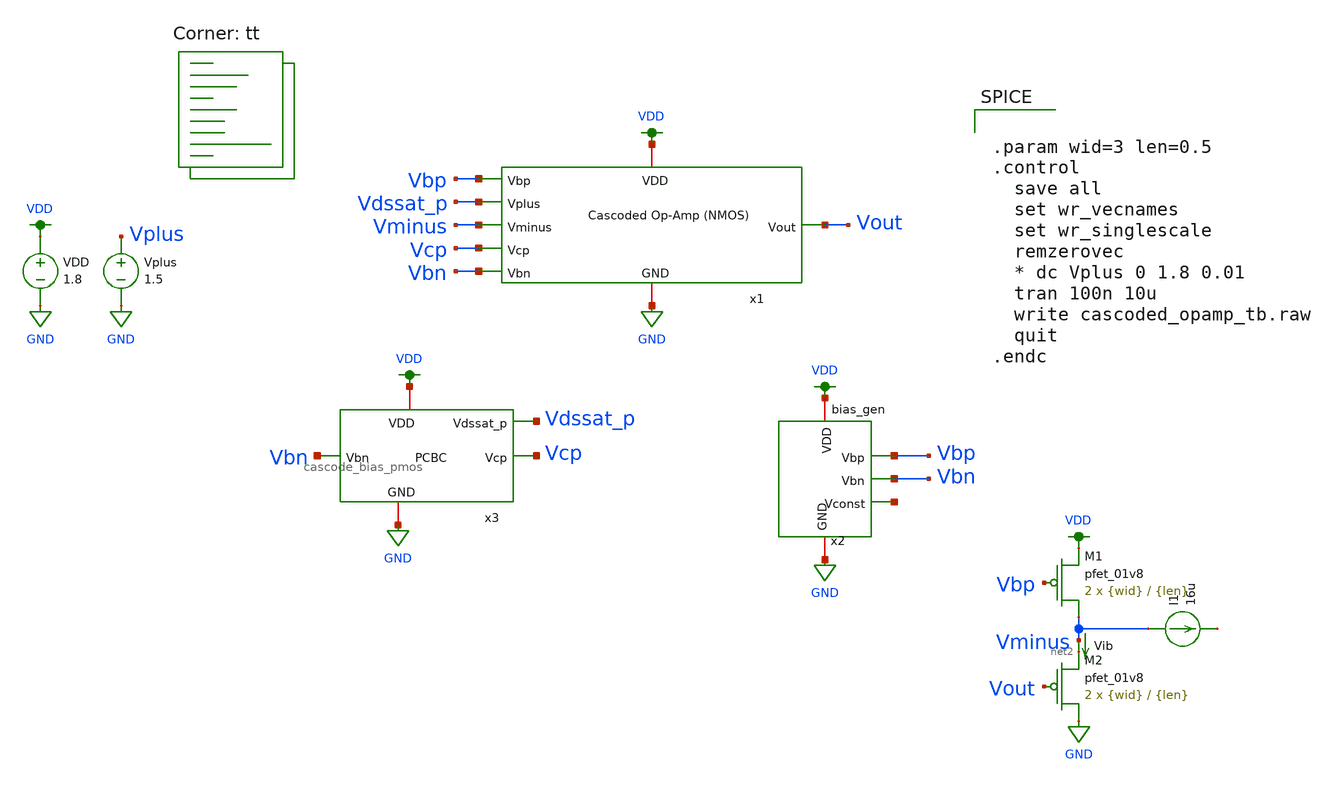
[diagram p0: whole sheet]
** sch_path: final/schematics/cascoded_opamp_tb.sch
**.subckt cascoded_opamp_tb
x1 Vbp Vdssat_p Vminus Vcp Vbn VDD GND Vout cascoded_opamp
VDD VDD GND 1.8
x3 Vbn VDD GND Vcp Vdssat_p cascode_bias_pmos
x2 VDD Vbp net1 GND Vbn bias_gen
XM1 Vminus Vbp VDD VDD sky130_fd_pr__pfet_01v8 L={len} W={wid} nf=1 ad='int((nf+1)/2) * W/nf * 0.29'
+ as='int((nf+2)/2) * W/nf * 0.29' pd='2*int((nf+1)/2) * (W/nf + 0.29)' ps='2*int((nf+2)/2) * (W/nf + 0.29)'
+ nrd='0.29 / W' nrs='0.29 / W' sa=0 sb=0 sd=0 mult=2 m=2
XM2 GND Vout net2 VDD sky130_fd_pr__pfet_01v8 L={len} W={wid} nf=1 ad='int((nf+1)/2) * W/nf * 0.29' as='int((nf+2)/2) * W/nf * 0.29'
+ pd='2*int((nf+1)/2) * (W/nf + 0.29)' ps='2*int((nf+2)/2) * (W/nf + 0.29)' nrd='0.29 / W' nrs='0.29 / W'
+ sa=0 sb=0 sd=0 mult=2 m=2
Vib Vminus net2 0
.save i(vib)
Vplus Vplus GND 1.5
I1 Vminus net3 16u
**** begin user architecture code
.lib $::SKYWATER_MODELS/sky130.lib.spice tt


.param wid=3 len=0.5
.control
  save all
  set wr_vecnames
  set wr_singlescale
  remzerovec
  * dc Vplus 0 1.8 0.01
  tran 100n 10u
  write cascoded_opamp_tb.raw
  quit
.endc


**** end user architecture code
**.ends

* expanding   symbol:  cascoded_opamp.sym # of pins=8
** sym_path: final/schematics/cascoded_opamp.sym
** sch_path: final/schematics/cascoded_opamp.sch
.subckt cascoded_opamp Vbp Vplus Vminus Vcp Vbn VDD GND Vout
*.ipin Vbp
*.ipin Vplus
*.ipin Vminus
*.ipin Vcp
*.ipin Vbn
*.iopin VDD
*.iopin GND
*.opin Vout
XM1 net1 Vbn GND GND sky130_fd_pr__nfet_01v8 L=0.15 W=1 nf=1 ad='int((nf+1)/2) * W/nf * 0.29' as='int((nf+2)/2) * W/nf * 0.29'
+ pd='2*int((nf+1)/2) * (W/nf + 0.29)' ps='2*int((nf+2)/2) * (W/nf + 0.29)' nrd='0.29 / W' nrs='0.29 / W'
+ sa=0 sb=0 sd=0 mult=1 m=1
XM2 net2 Vminus net1 GND sky130_fd_pr__nfet_01v8 L=0.15 W=1 nf=1 ad='int((nf+1)/2) * W/nf * 0.29' as='int((nf+2)/2) * W/nf * 0.29'
+ pd='2*int((nf+1)/2) * (W/nf + 0.29)' ps='2*int((nf+2)/2) * (W/nf + 0.29)' nrd='0.29 / W' nrs='0.29 / W'
+ sa=0 sb=0 sd=0 mult=1 m=1
XM3 net1 Vplus net3 GND sky130_fd_pr__nfet_01v8 L=0.15 W=1 nf=1 ad='int((nf+1)/2) * W/nf * 0.29' as='int((nf+2)/2) * W/nf * 0.29'
+ pd='2*int((nf+1)/2) * (W/nf + 0.29)' ps='2*int((nf+2)/2) * (W/nf + 0.29)' nrd='0.29 / W' nrs='0.29 / W'
+ sa=0 sb=0 sd=0 mult=1 m=1
XM4 net2 Vbp VDD VDD sky130_fd_pr__pfet_01v8 L=0.15 W=1 nf=1 ad='int((nf+1)/2) * W/nf * 0.29' as='int((nf+2)/2) * W/nf * 0.29'
+ pd='2*int((nf+1)/2) * (W/nf + 0.29)' ps='2*int((nf+2)/2) * (W/nf + 0.29)' nrd='0.29 / W' nrs='0.29 / W'
+ sa=0 sb=0 sd=0 mult=1 m=1
XM5 net3 Vbp VDD VDD sky130_fd_pr__pfet_01v8 L=0.15 W=1 nf=1 ad='int((nf+1)/2) * W/nf * 0.29' as='int((nf+2)/2) * W/nf * 0.29'
+ pd='2*int((nf+1)/2) * (W/nf + 0.29)' ps='2*int((nf+2)/2) * (W/nf + 0.29)' nrd='0.29 / W' nrs='0.29 / W'
+ sa=0 sb=0 sd=0 mult=1 m=1
XM6 net4 Vcp net2 VDD sky130_fd_pr__pfet_01v8 L=0.15 W=1 nf=1 ad='int((nf+1)/2) * W/nf * 0.29' as='int((nf+2)/2) * W/nf * 0.29'
+ pd='2*int((nf+1)/2) * (W/nf + 0.29)' ps='2*int((nf+2)/2) * (W/nf + 0.29)' nrd='0.29 / W' nrs='0.29 / W'
+ sa=0 sb=0 sd=0 mult=1 m=1
XM7 Vout Vcp net3 VDD sky130_fd_pr__pfet_01v8 L=0.15 W=1 nf=1 ad='int((nf+1)/2) * W/nf * 0.29' as='int((nf+2)/2) * W/nf * 0.29'
+ pd='2*int((nf+1)/2) * (W/nf + 0.29)' ps='2*int((nf+2)/2) * (W/nf + 0.29)' nrd='0.29 / W' nrs='0.29 / W'
+ sa=0 sb=0 sd=0 mult=1 m=1
XM8 GND net4 net4 GND sky130_fd_pr__nfet_01v8 L=0.15 W=1 nf=1 ad='int((nf+1)/2) * W/nf * 0.29' as='int((nf+2)/2) * W/nf * 0.29'
+ pd='2*int((nf+1)/2) * (W/nf + 0.29)' ps='2*int((nf+2)/2) * (W/nf + 0.29)' nrd='0.29 / W' nrs='0.29 / W'
+ sa=0 sb=0 sd=0 mult=1 m=1
XM9 Vout net4 GND GND sky130_fd_pr__nfet_01v8 L=0.15 W=1 nf=1 ad='int((nf+1)/2) * W/nf * 0.29' as='int((nf+2)/2) * W/nf * 0.29'
+ pd='2*int((nf+1)/2) * (W/nf + 0.29)' ps='2*int((nf+2)/2) * (W/nf + 0.29)' nrd='0.29 / W' nrs='0.29 / W'
+ sa=0 sb=0 sd=0 mult=1 m=1
.ends


* expanding   symbol:  cascode_bias_pmos.sym # of pins=5
** sym_path: final/schematics/cascode_bias_pmos.sym
** sch_path: final/schematics/cascode_bias_pmos.sch
.subckt cascode_bias_pmos Vbn VDD GND Vcp Vdssat_p
*.ipin Vbn
*.iopin VDD
*.iopin GND
*.opin Vcp
*.opin Vdssat_p
XM1 VDD net1 Vdssat_p VDD sky130_fd_pr__pfet_01v8 L={len} W={wid} nf=1 ad='int((nf+1)/2) * W/nf * 0.29'
+ as='int((nf+2)/2) * W/nf * 0.29' pd='2*int((nf+1)/2) * (W/nf + 0.29)' ps='2*int((nf+2)/2) * (W/nf + 0.29)'
+ nrd='0.29 / W' nrs='0.29 / W' sa=0 sb=0 sd=0 mult=1 m=1
XM2 Vdssat_p net1 net1 VDD sky130_fd_pr__pfet_01v8 L={len} W={wid} nf=1 ad='int((nf+1)/2) * W/nf * 0.29'
+ as='int((nf+2)/2) * W/nf * 0.29' pd='2*int((nf+1)/2) * (W/nf + 0.29)' ps='2*int((nf+2)/2) * (W/nf + 0.29)'
+ nrd='0.29 / W' nrs='0.29 / W' sa=0 sb=0 sd=0 mult=1 m=1
XM3 Vdssat_p net1 net1 VDD sky130_fd_pr__pfet_01v8 L={len} W={wid} nf=1 ad='int((nf+1)/2) * W/nf * 0.29'
+ as='int((nf+2)/2) * W/nf * 0.29' pd='2*int((nf+1)/2) * (W/nf + 0.29)' ps='2*int((nf+2)/2) * (W/nf + 0.29)'
+ nrd='0.29 / W' nrs='0.29 / W' sa=0 sb=0 sd=0 mult=1 m=1
XM4 Vdssat_p Vcp Vcp VDD sky130_fd_pr__pfet_01v8 L={len} W={wid} nf=1 ad='int((nf+1)/2) * W/nf * 0.29'
+ as='int((nf+2)/2) * W/nf * 0.29' pd='2*int((nf+1)/2) * (W/nf + 0.29)' ps='2*int((nf+2)/2) * (W/nf + 0.29)'
+ nrd='0.29 / W' nrs='0.29 / W' sa=0 sb=0 sd=0 mult=1 m=1
XM5 net2 Vbn net1 GND sky130_fd_pr__nfet_01v8 L={len} W={wid} nf=1 ad='int((nf+1)/2) * W/nf * 0.29' as='int((nf+2)/2) * W/nf * 0.29'
+ pd='2*int((nf+1)/2) * (W/nf + 0.29)' ps='2*int((nf+2)/2) * (W/nf + 0.29)' nrd='0.29 / W' nrs='0.29 / W'
+ sa=0 sb=0 sd=0 mult=1 m=1
XM6 net3 Vbn net2 GND sky130_fd_pr__nfet_01v8 L={len} W={wid} nf=1 ad='int((nf+1)/2) * W/nf * 0.29' as='int((nf+2)/2) * W/nf * 0.29'
+ pd='2*int((nf+1)/2) * (W/nf + 0.29)' ps='2*int((nf+2)/2) * (W/nf + 0.29)' nrd='0.29 / W' nrs='0.29 / W'
+ sa=0 sb=0 sd=0 mult=1 m=1
XM7 GND Vbn net3 GND sky130_fd_pr__nfet_01v8 L={len} W={wid} nf=1 ad='int((nf+1)/2) * W/nf * 0.29' as='int((nf+2)/2) * W/nf * 0.29'
+ pd='2*int((nf+1)/2) * (W/nf + 0.29)' ps='2*int((nf+2)/2) * (W/nf + 0.29)' nrd='0.29 / W' nrs='0.29 / W'
+ sa=0 sb=0 sd=0 mult=1 m=1
XM8 GND Vbn Vcp GND sky130_fd_pr__nfet_01v8 L={len} W={wid} nf=1 ad='int((nf+1)/2) * W/nf * 0.29' as='int((nf+2)/2) * W/nf * 0.29'
+ pd='2*int((nf+1)/2) * (W/nf + 0.29)' ps='2*int((nf+2)/2) * (W/nf + 0.29)' nrd='0.29 / W' nrs='0.29 / W'
+ sa=0 sb=0 sd=0 mult=1 m=1
**** begin user architecture code

.param len=0.5 wid=3

**** end user architecture code
.ends


* expanding   symbol:  /home/dt/Documents/madvlsi/final/schematics/bias_gen/bias_gen.sym # of pins=5
** sym_path: final/schematics/bias_gen/bias_gen.sym
** sch_path: final/schematics/bias_gen/bias_gen.sch
.subckt bias_gen VDD Vbp Vconst GND Vbn
*.iopin VDD
*.opin Vbp
*.iopin GND
*.opin Vbn
*.opin Vconst
**** begin user architecture code

.param len=0.5 wid=3

**** end user architecture code
XM10 Vconst net1 net1 GND sky130_fd_pr__nfet_01v8 L={len} W={wid} nf=1 ad='int((nf+1)/2) * W/nf * 0.29'
+ as='int((nf+2)/2) * W/nf * 0.29' pd='2*int((nf+1)/2) * (W/nf + 0.29)' ps='2*int((nf+2)/2) * (W/nf + 0.29)'
+ nrd='0.29 / W' nrs='0.29 / W' sa=0 sb=0 sd=0 mult=10 m=10
XM11 Vbn Vbn GND GND sky130_fd_pr__nfet_01v8 L={len} W={wid} nf=1 ad='int((nf+1)/2) * W/nf * 0.29' as='int((nf+2)/2) * W/nf * 0.29'
+ pd='2*int((nf+1)/2) * (W/nf + 0.29)' ps='2*int((nf+2)/2) * (W/nf + 0.29)' nrd='0.29 / W' nrs='0.29 / W'
+ sa=0 sb=0 sd=0 mult=1 m=1
XM12 GND Vbp GND GND sky130_fd_pr__nfet_01v8 L=10 W=10 nf=1 ad='int((nf+1)/2) * W/nf * 0.29' as='int((nf+2)/2) * W/nf * 0.29'
+ pd='2*int((nf+1)/2) * (W/nf + 0.29)' ps='2*int((nf+2)/2) * (W/nf + 0.29)' nrd='0.29 / W' nrs='0.29 / W'
+ sa=0 sb=0 sd=0 mult=1 m=1
XM13 VDD Vbp net1 VDD sky130_fd_pr__pfet_01v8 L={len} W={wid} nf=1 ad='int((nf+1)/2) * W/nf * 0.29' as='int((nf+2)/2) * W/nf * 0.29'
+ pd='2*int((nf+1)/2) * (W/nf + 0.29)' ps='2*int((nf+2)/2) * (W/nf + 0.29)' nrd='0.29 / W' nrs='0.29 / W'
+ sa=0 sb=0 sd=0 mult=1 m=1
XM14 GND Vbn Vbp GND sky130_fd_pr__nfet_01v8 L={len} W={wid} nf=1 ad='int((nf+1)/2) * W/nf * 0.29' as='int((nf+2)/2) * W/nf * 0.29'
+ pd='2*int((nf+1)/2) * (W/nf + 0.29)' ps='2*int((nf+2)/2) * (W/nf + 0.29)' nrd='0.29 / W' nrs='0.29 / W'
+ sa=0 sb=0 sd=0 mult=1 m=1
XM15 net2 net1 GND GND sky130_fd_pr__nfet_01v8 L={len} W={wid} nf=1 ad='int((nf+1)/2) * W/nf * 0.29'
+ as='int((nf+2)/2) * W/nf * 0.29' pd='2*int((nf+1)/2) * (W/nf + 0.29)' ps='2*int((nf+2)/2) * (W/nf + 0.29)'
+ nrd='0.29 / W' nrs='0.29 / W' sa=0 sb=0 sd=0 mult=1 m=1
XM16 VDD net2 net2 VDD sky130_fd_pr__pfet_01v8 L={len} W={wid} nf=1 ad='int((nf+1)/2) * W/nf * 0.29'
+ as='int((nf+2)/2) * W/nf * 0.29' pd='2*int((nf+1)/2) * (W/nf + 0.29)' ps='2*int((nf+2)/2) * (W/nf + 0.29)'
+ nrd='0.29 / W' nrs='0.29 / W' sa=0 sb=0 sd=0 mult=1 m=1
XM17 Vbp net2 VDD VDD sky130_fd_pr__pfet_01v8 L={len} W={wid} nf=1 ad='int((nf+1)/2) * W/nf * 0.29' as='int((nf+2)/2) * W/nf * 0.29'
+ pd='2*int((nf+1)/2) * (W/nf + 0.29)' ps='2*int((nf+2)/2) * (W/nf + 0.29)' nrd='0.29 / W' nrs='0.29 / W'
+ sa=0 sb=0 sd=0 mult=1 m=1
XM18 Vbn Vbp VDD VDD sky130_fd_pr__pfet_01v8 L={len} W={wid} nf=1 ad='int((nf+1)/2) * W/nf * 0.29' as='int((nf+2)/2) * W/nf * 0.29'
+ pd='2*int((nf+1)/2) * (W/nf + 0.29)' ps='2*int((nf+2)/2) * (W/nf + 0.29)' nrd='0.29 / W' nrs='0.29 / W'
+ sa=0 sb=0 sd=0 mult=1 m=1
XR2 GND Vconst GND sky130_fd_pr__res_high_po_0p35 L=9 mult=1 m=1
.ends

.GLOBAL VDD
.GLOBAL GND
.end
